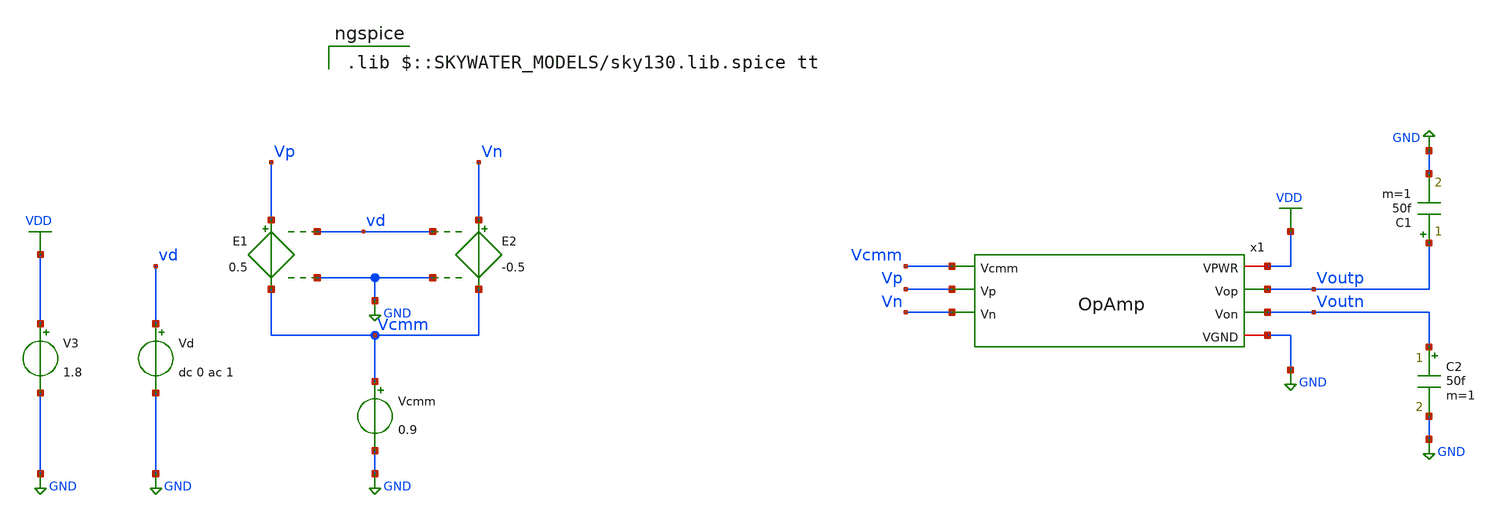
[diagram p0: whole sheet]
** sch_path: Circuits/MillerOpAmpCMMFB/OpAmp_tb.sch
**.subckt OpAmp_tb
V3 VDD GND 1.8
E1 Vp Vcmm vd GND 0.5
E2 Vn Vcmm vd GND -0.5
Vcmm Vcmm GND 0.9
Vd vd GND dc 0 ac 1
x1 VDD Vcmm Voutp Voutn Vp Vn GND OpAmp
C2 Voutn GND 50f m=1
C1 Voutp GND 50f m=1
**** begin user architecture code



* ngspice commands
.option savecurrents
.save all
.control
ac dec 1001 1 100Meg
let vod = V(Voutp)-V(Voutn)
meas ac gain max vod
let gain3dB = gain/sqrt(2)
meas ac BW TRIG at=1 TARG vod val=gain3dB fall=LAST
let GBW = BW*gain*1e-6
print GBW
print vodmax
plot vdb(vod) xlimit 1k 100Meg ylabel 'small signal gain'
let outd = 180/PI*cph(vod)
meas ac ftHz when vdb(vod)=1 fall=LAST
meas ac ph find outd when vdb(vod)=0 fall=LAST
let phm = ph+180
print phm
settype phase outd
plot outd xlimit 1k 100Meg ylabel 'phase'
dc Vd -0.02 0.02 1m
let vod = V(Voutp)-V(Voutn)
plot vod
op
write MillerOpAmp_tb.raw
.endc



 .lib $::SKYWATER_MODELS/sky130.lib.spice tt

**** end user architecture code
**.ends
.GLOBAL GND
.GLOBAL VDD
.end
